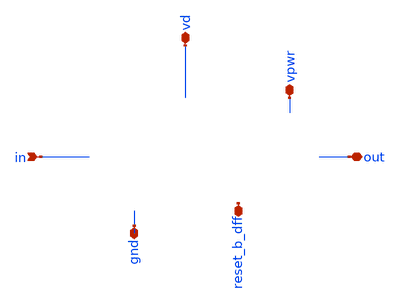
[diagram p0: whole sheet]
** sch_path: sigma-delta_modulator/xschem/sigma-delta-pex.sch
* Copyright 2020 Stefan Frederik Schippers
* Licensed under the Apache License, Version 2.0 (the "License");
* you may not use this file except in compliance with the License.
* You may obtain a copy of the License at
* https://www.apache.org/licenses/LICENSE-2.0
* Unless required by applicable law or agreed to in writing, software
* distributed under the License is distributed on an "AS IS" BASIS,
* WITHOUT WARRANTIES OR CONDITIONS OF ANY KIND, either express or implied.
* See the License for the specific language governing permissions and
* limitations under the License.
**.subckt sigma-delta-pex in gnd out reset_b_dff vpwr vd
*.ipin in
*.iopin gnd
*.iopin out
*.iopin reset_b_dff
*.iopin vpwr
*.iopin vd
**** begin user architecture code



* NGSPICE file created from sigma-delta.ext - technology: sky130A

*.subckt sigma-delta reset_b_dff gnd vd in clk vpwr out
X0 a_n1599_309# a_n1774_335# a_n1420_335# gnd.t15 sky130_fd_pr__nfet_01v8 ad=0.109 pd=1.36 as=0.064
+ ps=0.725 w=0.42 l=0.15
X1 a_n2266_4800# a_n2100_3468# gnd.t37 sky130_fd_pr__res_xhigh_po_0p35 l=4.5
X2 a_n1124_4800# a_n958_3468# gnd.t34 sky130_fd_pr__res_xhigh_po_0p35 l=4.5
X3 x1.Q a_n1599_309# vpwr.t19 vpwr.t18 sky130_fd_pr__pfet_01v8_hvt ad=0.28 pd=2.56 as=0.213 ps=1.67
+ w=1 l=0.15
X4 a_n2339_335# a_n2689_335# a_n2434_335# vpwr.t11 sky130_fd_pr__pfet_01v8_hvt ad=0.0724 pd=0.765
+ as=0.0651 ps=0.73 w=0.42 l=0.15
X5 a_n2121_577# a_n2339_335# vpwr.t13 vpwr.t12 sky130_fd_pr__pfet_01v8_hvt ad=0.129 pd=1.18 as=0.218
+ ps=2.2 w=0.84 l=0.15
X6 a_n1420_335# reset_b_dff.t0 gnd.t7 gnd.t6 sky130_fd_pr__nfet_01v8 ad=0.064 pd=0.725 as=0.125
+ ps=1.01 w=0.42 l=0.15
X7 a_n792_4800# a_n626_3468# gnd.t11 sky130_fd_pr__res_xhigh_po_0p35 l=4.5
X8 in_int gnd.t20 sky130_fd_pr__cap_mim_m3_2 l=27.2 w=27.2
X9 a_n2714_2632# a_n2880_1800# gnd.t19 sky130_fd_pr__res_xhigh_po_0p35 l=2
X10 out.t0 a_n1035_335# gnd.t33 gnd.t32 sky130_fd_pr__nfet_01v8 ad=0.169 pd=1.82 as=0.1 ps=0.985
+ w=0.65 l=0.15
X11 a_n1934_4800# a_n2100_3468# gnd.t35 sky130_fd_pr__res_xhigh_po_0p35 l=4.5
X12 in_comp a_n1884_1800# gnd.t45 sky130_fd_pr__res_xhigh_po_0p35 l=2
X13 a_n1612_701# a_n2689_335# a_n1774_335# vpwr.t10 sky130_fd_pr__pfet_01v8_hvt ad=0.0567 pd=0.69
+ as=0.0588 ps=0.7 w=0.42 l=0.15
X14 a_n2077_335# a_n2121_577# a_n2243_335# gnd.t18 sky130_fd_pr__nfet_01v8 ad=0.0441 pd=0.63 as=0.14
+ ps=1.1 w=0.42 l=0.15
X15 a_n2434_335# x1.D gnd.t17 gnd.t16 sky130_fd_pr__nfet_01v8 ad=0.066 pd=0.745 as=0.221 ps=1.89
+ w=0.42 l=0.15
X16 a_n1599_309# reset_b_dff.t1 vpwr.t1 vpwr.t0 sky130_fd_pr__pfet_01v8_hvt ad=0.0567 pd=0.69
+ as=0.0819 ps=0.81 w=0.42 l=0.15
X17 a_n2598_4800# a_n2764_3468# gnd.t36 sky130_fd_pr__res_xhigh_po_0p35 l=4.5
X18 a_n1665_335# a_n2855_335# a_n1774_335# gnd.t49 sky130_fd_pr__nfet_01v8 ad=0.0669 pd=0.75
+ as=0.0711 ps=0.755 w=0.36 l=0.15
X19 a_n1456_4800# in_int gnd.t14 sky130_fd_pr__res_xhigh_po_0p35 l=4.5
X20 gnd.t31 a_n1599_309# a_n1665_335# gnd.t30 sky130_fd_pr__nfet_01v8 ad=0.125 pd=1.01 as=0.0669
+ ps=0.75 w=0.42 l=0.15
X21 a_n2434_335# x1.D vpwr.t7 vpwr.t6 sky130_fd_pr__pfet_01v8_hvt ad=0.0651 pd=0.73 as=0.109 ps=1.36
+ w=0.42 l=0.15
X22 vpwr.t17 a_n1599_309# a_n1612_701# vpwr.t16 sky130_fd_pr__pfet_01v8_hvt ad=0.0819 pd=0.81
+ as=0.0567 ps=0.69 w=0.42 l=0.15
X23 vpwr.t5 a_n1774_335# a_n1599_309# vpwr.t4 sky130_fd_pr__pfet_01v8_hvt ad=0.213 pd=1.67 as=0.0567
+ ps=0.69 w=0.42 l=0.15
X24 a_n2121_577# a_n2339_335# gnd.t25 gnd.t24 sky130_fd_pr__nfet_01v8 ad=0.0999 pd=0.985 as=0.135
+ ps=1.15 w=0.64 l=0.15
X25 vpwr.t3 clk.t0 a_n2855_335# vpwr.t2 sky130_fd_pr__pfet_01v8_hvt ad=0.0864 pd=0.91 as=0.166
+ ps=1.8 w=0.64 l=0.15
X26 gnd.t53 reset_b_dff.t2 a_n2077_335# gnd.t52 sky130_fd_pr__nfet_01v8 ad=0.135 pd=1.15 as=0.0441
+ ps=0.63 w=0.42 l=0.15
X27 vpwr.t15 a_n1599_309# a_n1035_335# vpwr.t14 sky130_fd_pr__pfet_01v8_hvt ad=0.154 pd=1.34
+ as=0.166 ps=1.8 w=0.64 l=0.15
X28 gnd.t29 a_n1599_309# a_n1035_335# gnd.t28 sky130_fd_pr__nfet_01v8 ad=0.1 pd=0.985 as=0.109
+ ps=1.36 w=0.42 l=0.15
X29 a_n2266_4800# a_n2432_3468# gnd.t2 sky130_fd_pr__res_xhigh_po_0p35 l=4.5
X30 a_n2050_2632# a_n2216_1800# gnd.t1 sky130_fd_pr__res_xhigh_po_0p35 l=2
X31 gnd.t43 clk.t1 a_n2855_335# gnd.t42 sky130_fd_pr__nfet_01v8 ad=0.0567 pd=0.69 as=0.109 ps=1.36
+ w=0.42 l=0.15
X32 a_n2243_335# a_n2689_335# a_n2339_335# gnd.t23 sky130_fd_pr__nfet_01v8 ad=0.14 pd=1.1 as=0.0594
+ ps=0.69 w=0.36 l=0.15
X33 vd.t1 in_comp x1.D vd.t0 sky130_fd_pr__pfet_01v8 ad=0.87 pd=6.58 as=0.87 ps=6.58 w=3 l=0.15
X34 a_n1124_4800# a_n1290_3468# gnd.t44 sky130_fd_pr__res_xhigh_po_0p35 l=4.5
X35 a_n2339_335# a_n2855_335# a_n2434_335# gnd.t48 sky130_fd_pr__nfet_01v8 ad=0.0594 pd=0.69
+ as=0.066 ps=0.745 w=0.36 l=0.15
X36 a_n460_4800# x1.Q gnd.t0 sky130_fd_pr__res_xhigh_po_0p35 l=4.5
X37 a_n2689_335# a_n2855_335# vpwr.t27 vpwr.t26 sky130_fd_pr__pfet_01v8_hvt ad=0.166 pd=1.8
+ as=0.0864 ps=0.91 w=0.64 l=0.15
X38 a_n2231_701# a_n2855_335# a_n2339_335# vpwr.t25 sky130_fd_pr__pfet_01v8_hvt ad=0.116 pd=0.97
+ as=0.0724 ps=0.765 w=0.42 l=0.15
X39 a_n2689_335# a_n2855_335# gnd.t47 gnd.t46 sky130_fd_pr__nfet_01v8 ad=0.109 pd=1.36 as=0.0567
+ ps=0.69 w=0.42 l=0.15
X40 a_n1774_335# a_n2855_335# a_n2121_577# vpwr.t24 sky130_fd_pr__pfet_01v8_hvt ad=0.0588 pd=0.7
+ as=0.129 ps=1.18 w=0.42 l=0.15
X41 a_n2382_2632# a_n2548_1800# gnd.t41 sky130_fd_pr__res_xhigh_po_0p35 l=2
X42 in_int a_n2880_1800# gnd.t13 sky130_fd_pr__res_xhigh_po_0p35 l=2
X43 x1.Q a_n1599_309# gnd.t27 gnd.t26 sky130_fd_pr__nfet_01v8 ad=0.169 pd=1.82 as=0.169 ps=1.82
+ w=0.65 l=0.15
X44 a_n460_4800# a_n626_3468# gnd.t10 sky130_fd_pr__res_xhigh_po_0p35 l=4.5
X45 a_n2231_701# reset_b_dff.t3 vpwr.t23 vpwr.t22 sky130_fd_pr__pfet_01v8_hvt ad=0.109 pd=1.36
+ as=0.0703 ps=0.755 w=0.42 l=0.15
X46 a_n2930_4800# a_n2764_3468# gnd.t5 sky130_fd_pr__res_xhigh_po_0p35 l=4.5
X47 a_n2714_2632# a_n2548_1800# gnd.t9 sky130_fd_pr__res_xhigh_po_0p35 l=2
X48 gnd.t40 in_comp x1.D gnd.t39 sky130_fd_pr__nfet_01v8 ad=0.29 pd=2.58 as=0.29 ps=2.58 w=1 l=0.15
X49 a_n1934_4800# in_int gnd.t21 sky130_fd_pr__res_xhigh_po_0p35 l=4.5
X50 a_n792_4800# a_n958_3468# gnd.t8 sky130_fd_pr__res_xhigh_po_0p35 l=4.5
X51 vpwr.t9 a_n2121_577# a_n2231_701# vpwr.t8 sky130_fd_pr__pfet_01v8_hvt ad=0.0703 pd=0.755
+ as=0.116 ps=0.97 w=0.42 l=0.15
X52 a_n1774_335# a_n2689_335# a_n2121_577# gnd.t22 sky130_fd_pr__nfet_01v8 ad=0.0711 pd=0.755
+ as=0.0999 ps=0.985 w=0.36 l=0.15
X53 a_n2598_4800# a_n2432_3468# gnd.t3 sky130_fd_pr__res_xhigh_po_0p35 l=4.5
X54 a_n2382_2632# a_n2216_1800# gnd.t51 sky130_fd_pr__res_xhigh_po_0p35 l=2
X55 in_comp gnd.t38 sky130_fd_pr__cap_mim_m3_2 l=27.2 w=27.2
X56 a_n2930_4800# in.t0 gnd.t4 sky130_fd_pr__res_xhigh_po_0p35 l=4.5
X57 a_n1456_4800# a_n1290_3468# gnd.t50 sky130_fd_pr__res_xhigh_po_0p35 l=4.5
X58 a_n2050_2632# a_n1884_1800# gnd.t12 sky130_fd_pr__res_xhigh_po_0p35 l=2
X59 out.t1 a_n1035_335# vpwr.t21 vpwr.t20 sky130_fd_pr__pfet_01v8_hvt ad=0.26 pd=2.52 as=0.154
+ ps=1.34 w=1 l=0.15
R0 gnd.n76 gnd.n12 1527.78
R1 gnd.n9 gnd.n3 1273.6
R2 gnd.n10 gnd.n9 1263.33
R3 gnd.t32 gnd.n84 1127.78
R4 gnd.t46 gnd.t16 1049.58
R5 gnd.n84 gnd.n83 788.875
R6 gnd.t26 gnd.t28 773.808
R7 gnd.t15 gnd.t26 773.808
R8 gnd.t23 gnd.t18 683.255
R9 gnd.t30 gnd.t6 613.284
R10 gnd.t52 gnd.t24 543.312
R11 gnd.t22 gnd.t49 448.644
R12 gnd.t24 gnd.t22 407.485
R13 gnd.t28 gnd.t32 399.252
R14 gnd.t49 gnd.t30 395.137
R15 gnd.t48 gnd.t23 395.137
R16 gnd.t16 gnd.t48 391.021
R17 gnd.t6 gnd.t15 374.557
R18 gnd.t42 gnd.t46 345.745
R19 gnd.t18 gnd.t52 296.353
R20 gnd gnd.t42 267.541
R21 gnd.n12 gnd.t0 243.835
R22 gnd.n23 gnd.t17 215.036
R23 gnd.t0 gnd.t10 172.754
R24 gnd.t10 gnd.t11 172.754
R25 gnd.t11 gnd.t8 172.754
R26 gnd.t8 gnd.t34 172.754
R27 gnd.t34 gnd.t44 172.754
R28 gnd.t44 gnd.t50 172.754
R29 gnd.n7 gnd.t45 165.469
R30 gnd.n32 gnd.t27 154.317
R31 gnd.n81 gnd.n1 149.835
R32 gnd.n81 gnd.n80 149.835
R33 gnd.n34 gnd.n33 128.757
R34 gnd.t35 gnd.t1 120.719
R35 gnd.t37 gnd.t51 120.719
R36 gnd.t2 gnd.t41 120.719
R37 gnd.t3 gnd.t9 120.719
R38 gnd.t36 gnd.t19 120.719
R39 gnd.t5 gnd.t13 120.719
R40 gnd.n30 gnd.n29 116.754
R41 gnd.n62 gnd.n21 107.24
R42 gnd.n49 gnd.n48 107.24
R43 gnd.n7 gnd.t14 107.191
R44 gnd.n29 gnd.t7 100.001
R45 gnd.n80 gnd.n78 98.6358
R46 gnd.t21 gnd.n4 93.6618
R47 gnd.n48 gnd.t53 72.8576
R48 gnd.n29 gnd.t31 70.0005
R49 gnd.n48 gnd.t25 60.5809
R50 gnd.n33 gnd.t29 57.1434
R51 gnd.t45 gnd.t21 52.0346
R52 gnd.t12 gnd.t35 52.0346
R53 gnd.t1 gnd.t37 52.0346
R54 gnd.t51 gnd.t2 52.0346
R55 gnd.t41 gnd.t3 52.0346
R56 gnd.t9 gnd.t36 52.0346
R57 gnd.t19 gnd.t5 52.0346
R58 gnd.t13 gnd.t4 52.0346
R59 gnd.n21 gnd.t47 38.5719
R60 gnd.n21 gnd.t43 38.5719
R61 gnd.n37 gnd.n36 34.6358
R62 gnd.n38 gnd.n37 34.6358
R63 gnd.n42 gnd.n41 34.6358
R64 gnd.n43 gnd.n42 34.6358
R65 gnd.n43 gnd.n27 34.6358
R66 gnd.n47 gnd.n27 34.6358
R67 gnd.n51 gnd.n50 34.6358
R68 gnd.n51 gnd.n25 34.6358
R69 gnd.n55 gnd.n25 34.6358
R70 gnd.n56 gnd.n55 34.6358
R71 gnd.n57 gnd.n56 34.6358
R72 gnd.n61 gnd.n23 29.7417
R73 gnd.n36 gnd.n32 27.8593
R74 gnd.n4 gnd.t12 27.0582
R75 gnd.n33 gnd.t33 25.4291
R76 gnd.n63 gnd.n62 24.4919
R77 gnd.n62 gnd.n61 22.9652
R78 gnd.n38 gnd.n30 17.6946
R79 gnd.n16 gnd.t40 17.405
R80 gnd.n57 gnd.n23 14.6829
R81 gnd.n34 gnd.n32 10.9075
R82 gnd.n16 gnd.n15 9.33321
R83 gnd.n50 gnd.n49 7.90638
R84 gnd.n50 gnd.n26 4.6505
R85 gnd.n59 gnd.n23 4.6505
R86 gnd.n62 gnd.n22 4.6505
R87 gnd.n52 gnd.n51 4.6505
R88 gnd.n53 gnd.n25 4.6505
R89 gnd.n55 gnd.n54 4.6505
R90 gnd.n56 gnd.n24 4.6505
R91 gnd.n58 gnd.n57 4.6505
R92 gnd.n61 gnd.n60 4.6505
R93 gnd.n36 gnd.n35 4.6505
R94 gnd.n37 gnd.n31 4.6505
R95 gnd.n39 gnd.n38 4.6505
R96 gnd.n41 gnd.n40 4.6505
R97 gnd.n42 gnd.n28 4.6505
R98 gnd.n44 gnd.n43 4.6505
R99 gnd.n45 gnd.n27 4.6505
R100 gnd.n47 gnd.n46 4.6505
R101 gnd.n65 gnd.n20 4.5005
R102 gnd.n65 gnd.n64 4.5005
R103 gnd.n41 gnd.n30 2.63579
R104 gnd.n65 gnd.n19 2.25328
R105 gnd.n68 gnd.n67 1.93469
R106 gnd.n49 gnd.n47 1.88285
R107 gnd gnd.n66 1.72422
R108 gnd.n68 gnd 1.25931
R109 gnd.n69 gnd.n68 0.575502
R110 gnd.n78 gnd.n77 0.541165
R111 gnd.n77 gnd.n76 0.541165
R112 gnd.n75 gnd.n74 0.347269
R113 gnd.n76 gnd.n75 0.347269
R114 gnd.n67 gnd.t38 0.266467
R115 gnd.n35 gnd.n34 0.144332
R116 gnd.n35 gnd.n31 0.120292
R117 gnd.n39 gnd.n31 0.120292
R118 gnd.n40 gnd.n39 0.120292
R119 gnd.n40 gnd.n28 0.120292
R120 gnd.n44 gnd.n28 0.120292
R121 gnd.n45 gnd.n44 0.120292
R122 gnd.n46 gnd.n45 0.120292
R123 gnd.n46 gnd.n26 0.120292
R124 gnd.n52 gnd.n26 0.120292
R125 gnd.n53 gnd.n52 0.120292
R126 gnd.n54 gnd.n53 0.120292
R127 gnd.n54 gnd.n24 0.120292
R128 gnd.n58 gnd.n24 0.120292
R129 gnd.n59 gnd.n58 0.120292
R130 gnd.n60 gnd.n59 0.120292
R131 gnd.n60 gnd.n22 0.120292
R132 gnd.n1 gnd.n0 0.10956
R133 gnd.n0 gnd.t39 0.10956
R134 gnd.n80 gnd.n79 0.10956
R135 gnd.n73 gnd.n14 0.084913
R136 gnd.n14 gnd.n13 0.0845034
R137 gnd.n22 gnd.n20 0.0734167
R138 gnd.n82 gnd.n81 0.0425017
R139 gnd.n83 gnd.n82 0.0425017
R140 gnd.n64 gnd 0.0330521
R141 gnd.n20 gnd.n18 0.0265417
R142 gnd gnd.n63 0.0226354
R143 gnd.n19 gnd.n18 0.0114272
R144 gnd.n63 gnd.n19 0.0113582
R145 gnd.n66 gnd.n65 0.0110001
R146 gnd.n70 gnd.n16 0.00867757
R147 gnd.n70 gnd.n69 0.00634112
R148 gnd.n64 gnd 0.00570833
R149 gnd.n9 gnd.n8 0.00517349
R150 gnd.n8 gnd.n7 0.00517349
R151 gnd.n6 gnd.n5 0.00517349
R152 gnd.n7 gnd.n6 0.00517349
R153 gnd.n73 gnd.n72 0.00440917
R154 gnd.n3 gnd.n2 0.0043402
R155 gnd.n11 gnd.n10 0.0043402
R156 gnd.n12 gnd.n11 0.0043402
R157 gnd.n72 gnd.n71 0.00391284
R158 gnd.n71 gnd.n70 0.00391159
R159 gnd.n67 gnd.t20 0.00288363
R160 gnd.n66 gnd.n18 0.00100955
R161 gnd.n76 gnd.n73 0.00100353
R162 gnd.n69 gnd.n17 0.00051897
R163 vpwr.t26 vpwr.t6 790.188
R164 vpwr.t18 vpwr.t14 648.131
R165 vpwr.t22 vpwr.t12 583.023
R166 vpwr.n45 vpwr 548.548
R167 vpwr.n26 vpwr.t13 514.011
R168 vpwr.t4 vpwr.t18 485.358
R169 vpwr.t25 vpwr.t8 414.33
R170 vpwr.n2 vpwr.t7 375.277
R171 vpwr.t16 vpwr.t0 319.627
R172 vpwr.n20 vpwr.n9 311.957
R173 vpwr.n42 vpwr.n1 311.894
R174 vpwr.n29 vpwr.n28 309.18
R175 vpwr.t12 vpwr.t24 292.991
R176 vpwr.t11 vpwr.t25 292.991
R177 vpwr.n13 vpwr.n10 292.5
R178 vpwr.n15 vpwr.n14 292.5
R179 vpwr.t14 vpwr.t20 287.072
R180 vpwr.t8 vpwr.t22 287.072
R181 vpwr.t6 vpwr.t11 272.274
R182 vpwr.t24 vpwr.t10 254.518
R183 vpwr.t0 vpwr.t4 248.599
R184 vpwr.t10 vpwr.t16 248.599
R185 vpwr.t2 vpwr.t26 244.306
R186 vpwr vpwr.t2 186.556
R187 vpwr.n14 vpwr.n13 182.929
R188 vpwr.n12 vpwr.n11 148.689
R189 vpwr.n9 vpwr.t17 119.608
R190 vpwr.n28 vpwr.t9 93.81
R191 vpwr.n13 vpwr.t5 68.0124
R192 vpwr.n28 vpwr.t23 63.3219
R193 vpwr.n9 vpwr.t1 63.3219
R194 vpwr.n11 vpwr.t15 61.9158
R195 vpwr.n1 vpwr.t27 41.5552
R196 vpwr.n1 vpwr.t3 41.5552
R197 vpwr.n41 vpwr.n40 34.6358
R198 vpwr.n34 vpwr.n4 34.6358
R199 vpwr.n35 vpwr.n34 34.6358
R200 vpwr.n36 vpwr.n35 34.6358
R201 vpwr.n30 vpwr.n27 34.6358
R202 vpwr.n21 vpwr.n7 34.6358
R203 vpwr.n25 vpwr.n7 34.6358
R204 vpwr.n36 vpwr.n2 32.377
R205 vpwr.n26 vpwr.n25 32.0005
R206 vpwr.n11 vpwr.t21 30.239
R207 vpwr.n20 vpwr.n19 30.1181
R208 vpwr.n14 vpwr.t19 29.316
R209 vpwr.n42 vpwr.n41 22.9652
R210 vpwr.n21 vpwr.n20 20.3299
R211 vpwr.n40 vpwr.n2 18.0711
R212 vpwr.n15 vpwr.n12 13.9946
R213 vpwr.n19 vpwr.n10 12.8758
R214 vpwr.n27 vpwr.n26 9.41227
R215 vpwr.n29 vpwr.n4 6.02403
R216 vpwr.n16 vpwr.n15 5.00414
R217 vpwr.n20 vpwr.n8 4.6505
R218 vpwr.n26 vpwr.n6 4.6505
R219 vpwr.n38 vpwr.n2 4.6505
R220 vpwr.n17 vpwr.n16 4.6505
R221 vpwr.n19 vpwr.n18 4.6505
R222 vpwr.n22 vpwr.n21 4.6505
R223 vpwr.n23 vpwr.n7 4.6505
R224 vpwr.n25 vpwr.n24 4.6505
R225 vpwr.n27 vpwr.n5 4.6505
R226 vpwr.n31 vpwr.n30 4.6505
R227 vpwr.n32 vpwr.n4 4.6505
R228 vpwr.n34 vpwr.n33 4.6505
R229 vpwr.n35 vpwr.n3 4.6505
R230 vpwr.n37 vpwr.n36 4.6505
R231 vpwr.n40 vpwr.n39 4.6505
R232 vpwr.n41 vpwr.n0 4.6505
R233 vpwr.n16 vpwr.n10 4.07323
R234 vpwr.n43 vpwr.n42 3.93272
R235 vpwr.n30 vpwr.n29 3.76521
R236 vpwr vpwr.n51 0.223
R237 vpwr.n17 vpwr.n12 0.144332
R238 vpwr.n43 vpwr.n0 0.138831
R239 vpwr.n18 vpwr.n17 0.120292
R240 vpwr.n18 vpwr.n8 0.120292
R241 vpwr.n22 vpwr.n8 0.120292
R242 vpwr.n23 vpwr.n22 0.120292
R243 vpwr.n24 vpwr.n23 0.120292
R244 vpwr.n24 vpwr.n6 0.120292
R245 vpwr.n6 vpwr.n5 0.120292
R246 vpwr.n31 vpwr.n5 0.120292
R247 vpwr.n32 vpwr.n31 0.120292
R248 vpwr.n33 vpwr.n32 0.120292
R249 vpwr.n33 vpwr.n3 0.120292
R250 vpwr.n37 vpwr.n3 0.120292
R251 vpwr.n38 vpwr.n37 0.120292
R252 vpwr.n39 vpwr.n38 0.120292
R253 vpwr.n39 vpwr.n0 0.120292
R254 vpwr.n44 vpwr.n43 0.107496
R255 vpwr.n47 vpwr 0.088
R256 vpwr.n51 vpwr.n50 0.0197304
R257 vpwr.n44 vpwr 0.0174271
R258 vpwr vpwr.n44 0.01675
R259 vpwr.n48 vpwr.n47 0.013
R260 vpwr.n50 vpwr.n49 0.00412567
R261 vpwr.n49 vpwr.n48 0.003625
R262 vpwr.n50 vpwr.n45 0.0015496
R263 vpwr.n49 vpwr.n46 0.000543305
R264 reset_b_dff.n14 reset_b_dff.t3 413.313
R265 reset_b_dff.n7 reset_b_dff.t1 344.005
R266 reset_b_dff.n6 reset_b_dff.t0 187.321
R267 reset_b_dff.n7 reset_b_dff.n5 152
R268 reset_b_dff.n14 reset_b_dff.t2 126.127
R269 reset_b_dff.n6 reset_b_dff.n1 73.2067
R270 reset_b_dff reset_b_dff.n4 14.0185
R271 reset_b_dff.n11 reset_b_dff.n10 9.3005
R272 reset_b_dff.n8 reset_b_dff.n2 9.3005
R273 reset_b_dff.n8 reset_b_dff.n7 9.3005
R274 reset_b_dff.n7 reset_b_dff.n6 9.15991
R275 reset_b_dff.n15 reset_b_dff.n14 7.02742
R276 reset_b_dff.n4 reset_b_dff 4.7293
R277 reset_b_dff.n9 reset_b_dff.n0 4.6505
R278 reset_b_dff.n18 reset_b_dff.n17 4.6505
R279 reset_b_dff.n4 reset_b_dff 4.53383
R280 reset_b_dff.n5 reset_b_dff 3.11401
R281 reset_b_dff.n17 reset_b_dff.n15 3.0725
R282 reset_b_dff.n24 reset_b_dff 2.98033
R283 reset_b_dff.n12 reset_b_dff 2.36657
R284 reset_b_dff.n5 reset_b_dff.n1 1.55726
R285 reset_b_dff.n10 reset_b_dff.n9 1.55726
R286 reset_b_dff.n8 reset_b_dff.n1 1.38428
R287 reset_b_dff.n9 reset_b_dff.n8 1.38428
R288 reset_b_dff.n10 reset_b_dff 1.38428
R289 reset_b_dff.n17 reset_b_dff.n16 1.2805
R290 reset_b_dff.n12 reset_b_dff 0.580857
R291 reset_b_dff.n3 reset_b_dff 0.196446
R292 reset_b_dff.n20 reset_b_dff 0.171696
R293 reset_b_dff.n20 reset_b_dff.n19 0.0901739
R294 reset_b_dff.n21 reset_b_dff.n20 0.0500874
R295 reset_b_dff.n13 reset_b_dff.n12 0.0466957
R296 reset_b_dff.n26 reset_b_dff.n25 0.0435328
R297 reset_b_dff.n18 reset_b_dff.n13 0.0331087
R298 reset_b_dff.n3 reset_b_dff.n2 0.02675
R299 reset_b_dff reset_b_dff.n11 0.0255
R300 reset_b_dff.n22 reset_b_dff.n21 0.0213989
R301 reset_b_dff.n24 reset_b_dff.n23 0.018111
R302 reset_b_dff.n19 reset_b_dff.n18 0.014087
R303 reset_b_dff.n25 reset_b_dff.n22 0.0127951
R304 reset_b_dff.n11 reset_b_dff.n0 0.01175
R305 reset_b_dff.n2 reset_b_dff.n0 0.0105
R306 reset_b_dff reset_b_dff.n3 0.00725676
R307 reset_b_dff reset_b_dff.n26 0.00459836
R308 reset_b_dff.n25 reset_b_dff.n24 0.0016109
R309 out.n0 out.t1 250.94
R310 out out.t0 144.601
R311 out.n0 out 4.7225
R312 out out.n0 3.35288
R313 clk.n3 clk.t0 294.557
R314 clk.n3 clk.t1 211.01
R315 clk.n4 clk.n3 8.28655
R316 clk.n2 clk 7.73487
R317 clk.n4 clk.n2 1.82961
R318 clk clk.n5 0.981259
R319 clk.n5 clk.n4 0.848973
R320 clk.n0 clk 0.385917
R321 clk.n1 clk.n0 0.03175
R322 clk.n2 clk.n1 0.00111796
R323 vd.n10 vd.n7 135.465
R324 vd.n13 vd.n12 101.647
R325 vd.n26 vd.t1 9.52337
R326 vd vd.n35 4.20467
R327 vd.n14 vd.n13 0.130052
R328 vd.n15 vd.n14 0.130052
R329 vd.n5 vd.n4 0.107375
R330 vd.n15 vd.n5 0.107375
R331 vd.n31 vd.n29 0.0456031
R332 vd.n25 vd.n23 0.0456031
R333 vd.n23 vd.n21 0.0456031
R334 vd.n34 vd.n33 0.0391598
R335 vd.n33 vd.n31 0.0391598
R336 vd.n12 vd.n11 0.0349892
R337 vd.n11 vd.t0 0.0349892
R338 vd.n9 vd.n8 0.0349892
R339 vd.n10 vd.n9 0.0333079
R340 vd.n26 vd.n25 0.0217629
R341 vd.n29 vd.n27 0.0198299
R342 vd.n16 vd.n3 0.0125538
R343 vd.n3 vd.n2 0.0120596
R344 vd.n7 vd.n6 0.00627981
R345 vd.n27 vd.n26 0.00501031
R346 vd.t0 vd.n10 0.00318081
R347 vd.n17 vd.n16 0.0018171
R348 vd.n18 vd.n17 0.00131751
R349 vd.n27 vd.n18 0.00131744
R350 vd.n33 vd.n32 0.00119114
R351 vd.n34 vd.n0 0.00101609
R352 vd.n16 vd.n15 0.00100038
R353 vd.n21 vd.n20 0.00100009
R354 vd.n29 vd.n28 0.000659706
R355 vd.n23 vd.n22 0.000659706
R356 vd.n31 vd.n1 0.000543686
R357 vd.n25 vd.n19 0.000543686
R358 vd.n35 vd.n34 0.000507883
R359 vd.n25 vd.n24 0.000507883
R360 vd.n31 vd.n30 0.000507883
R361 in in.t0 9.56433
C0 a_n1774_335# a_n2121_577# 0.0512f
C1 a_n2548_1800# a_n2714_2632# 0.00938f
C2 a_n1774_335# reset_b_dff 0.239f
C3 a_n1774_335# x1.D 9.45e-19
C4 in a_n2930_4800# 0.0056f
C5 a_n1599_309# reset_b_dff 0.28f
C6 a_n2121_577# vpwr 0.205f
C7 a_n1599_309# x1.D 0.004f
C8 reset_b_dff vpwr 0.205f
C9 a_n2339_335# a_n1774_335# 7.99e-20
C10 x1.D vpwr 0.238f
C11 a_n1124_4800# in_int 0.00765f
C12 a_n2382_2632# in_int 0.0613f
C13 in_comp a_n958_3468# 7.16e-19
C14 a_n1774_335# a_n1612_701# 0.00645f
C15 vd in_comp 0.833f
C16 a_n2339_335# vpwr 0.197f
C17 a_n2548_1800# a_n2880_1800# 0.296f
C18 a_n460_4800# x1.Q 0.00839f
C19 a_n2121_577# a_n1665_335# 4.2e-19
C20 a_n2689_335# a_n1774_335# 0.125f
C21 a_n1612_701# vpwr 7.36e-19
C22 a_n2266_4800# a_n2432_3468# 0.00473f
C23 reset_b_dff a_n1665_335# 7.93e-19
C24 a_n1774_335# out 6.85e-19
C25 x1.D a_n1665_335# 2.42e-20
C26 a_n2598_4800# a_n2432_3468# 0.00482f
C27 a_n1599_309# a_n2689_335# 0.0426f
C28 a_n1599_309# out 0.00735f
C29 a_n2689_335# vpwr 0.57f
C30 x1.Q a_n958_3468# 5e-20
C31 vpwr out 0.584f
C32 x1.Q a_n792_4800# 0.0032f
C33 out a_n2714_2632# 0.00336f
C34 a_n2434_335# clk 3.09e-19
C35 a_n2050_2632# in_comp 0.297f
C36 x1.Q vd 0.186f
C37 reset_b_dff a_n1035_335# 0.00144f
C38 x1.D a_n1035_335# 0.00209f
C39 a_n2855_335# a_n2548_1800# 2.33e-20
C40 x1.Q a_n626_3468# 0.414f
C41 a_n2050_2632# a_n2216_1800# 0.00938f
C42 a_n2548_1800# in_int 0.00497f
C43 a_n1290_3468# a_n958_3468# 0.312f
C44 a_n2100_3468# a_n2432_3468# 0.302f
C45 clk a_n1420_335# 6.32e-21
C46 a_n2855_335# a_n2121_577# 0.0701f
C47 a_n1290_3468# vd 0.00171f
C48 a_n2689_335# a_n1665_335# 2.36e-20
C49 a_n2930_4800# in_int 0.00283f
C50 a_n2855_335# reset_b_dff 0.312f
C51 a_n2434_335# x1.Q 7.58e-20
C52 a_n2855_335# x1.D 0.195f
C53 x1.D in_int 0.0121f
C54 in a_n2432_3468# 4.07e-20
C55 x1.Q a_n2050_2632# 2.81e-19
C56 a_n2880_1800# out 0.0144f
C57 in_comp a_n2216_1800# 4.76e-19
C58 a_n2382_2632# a_n2548_1800# 0.00938f
C59 a_n2689_335# a_n1035_335# 2.01e-19
C60 a_n2339_335# a_n2855_335# 0.115f
C61 a_n1884_1800# a_n2855_335# 1.47e-19
C62 x1.Q a_n1420_335# 6.05e-19
C63 a_n1035_335# out 0.0691f
C64 a_n1884_1800# in_int 0.00497f
C65 x1.Q in_comp 0.425f
C66 clk a_n2077_335# 1.82e-20
C67 a_n2689_335# a_n2855_335# 0.906f
C68 a_n2855_335# out 0.00153f
C69 x1.Q a_n2216_1800# 4.28e-19
C70 a_n2855_335# a_n2243_335# 0.00134f
C71 out in_int 0.0102f
C72 a_n2598_4800# a_n2764_3468# 0.00434f
C73 x1.Q a_n2077_335# 9.75e-20
C74 a_n1774_335# vd 3.52e-19
C75 a_n1599_309# vd 0.00172f
C76 a_n2382_2632# out 0.00336f
C77 vd vpwr 0.00696f
C78 x1.D a_n2548_1800# 3.98e-19
C79 a_n2432_3468# in_int 0.0411f
C80 x1.Q a_n1290_3468# 1.87e-20
C81 a_n2100_3468# a_n2050_2632# 0.00472f
C82 x1.Q a_n2231_701# 3.66e-19
C83 reset_b_dff a_n2121_577# 0.172f
C84 in a_n2764_3468# 0.303f
C85 x1.D a_n2121_577# 6.24e-19
C86 a_n2434_335# vpwr 0.0827f
C87 vd a_n1456_4800# 5.85e-19
C88 a_n2764_3468# a_n2714_2632# 0.00472f
C89 reset_b_dff x1.D 0.223f
C90 vd a_n1934_4800# 6.34e-20
C91 a_n2339_335# a_n2121_577# 0.21f
C92 a_n1599_309# a_n1420_335# 0.0074f
C93 a_n2382_2632# a_n2432_3468# 0.00472f
C94 a_n2339_335# reset_b_dff 0.165f
C95 a_n2689_335# a_n2548_1800# 1.47e-19
C96 a_n2339_335# x1.D 0.00353f
C97 a_n1612_701# a_n2121_577# 2.6e-19
C98 a_n1774_335# in_comp 5.26e-20
C99 a_n460_4800# in_int 0.0109f
C100 a_n2548_1800# out 0.0144f
C101 vd a_n1035_335# 0.00317f
C102 reset_b_dff a_n1612_701# 2.06e-19
C103 a_n1612_701# x1.D 2.11e-20
C104 a_n1774_335# clk 6.46e-20
C105 a_n1599_309# in_comp 0.00158f
C106 a_n2689_335# a_n2121_577# 0.186f
C107 a_n1884_1800# a_n2339_335# 1.87e-19
C108 in_comp vpwr 0.00229f
C109 in_comp a_n2714_2632# 1.21e-19
C110 a_n1599_309# clk 2.68e-20
C111 a_n2121_577# out 3.73e-19
C112 a_n2689_335# reset_b_dff 0.0304f
C113 a_n2689_335# x1.D 0.229f
C114 a_n2243_335# a_n2121_577# 3.16e-19
C115 reset_b_dff out 0.00564f
C116 clk vpwr 0.19f
C117 x1.D out 0.294f
C118 vd a_n2855_335# 1.72e-20
C119 a_n2243_335# reset_b_dff 0.00292f
C120 in_int a_n958_3468# 0.0509f
C121 a_n792_4800# in_int 0.00675f
C122 a_n2243_335# x1.D 8.22e-19
C123 x1.Q a_n2100_3468# 1.43e-21
C124 vd in_int 0.304f
C125 a_n1774_335# x1.Q 0.00593f
C126 a_n2689_335# a_n2339_335# 0.23f
C127 in_int a_n626_3468# 0.0178f
C128 a_n1884_1800# a_n2689_335# 1.07e-19
C129 a_n2339_335# out 7.05e-19
C130 a_n1884_1800# out 0.0144f
C131 a_n1599_309# x1.Q 0.142f
C132 a_n2689_335# a_n1612_701# 1.46e-19
C133 a_n2339_335# a_n2243_335# 0.0138f
C134 a_n2266_4800# a_n2598_4800# 0.303f
C135 x1.Q vpwr 0.175f
C136 a_n2434_335# a_n2855_335# 0.0931f
C137 clk a_n1665_335# 1.1e-20
C138 a_n1124_4800# a_n958_3468# 0.00509f
C139 a_n1124_4800# a_n792_4800# 0.307f
C140 a_n2764_3468# in_int 0.0408f
C141 vd a_n1124_4800# 0.00116f
C142 clk a_n2880_1800# 1.96e-19
C143 a_n2689_335# out 0.0011f
C144 in_comp a_n1035_335# 0.00219f
C145 in a_n1290_3468# 9.87e-22
C146 a_n2050_2632# in_int 0.0597f
C147 a_n2689_335# a_n2243_335# 2.28e-19
C148 vpwr a_n2231_701# 0.143f
C149 x1.Q a_n1665_335# 1.47e-19
C150 a_n2266_4800# a_n2100_3468# 0.00473f
C151 in_comp a_n2855_335# 2.02e-20
C152 in_comp in_int 1.13f
C153 a_n1290_3468# a_n1456_4800# 0.00473f
C154 a_n2382_2632# a_n2050_2632# 0.296f
C155 clk a_n2855_335# 0.273f
C156 x1.Q a_n1035_335# 0.226f
C157 a_n2216_1800# in_int 0.00497f
C158 x1.Q a_n2855_335# 9.54e-19
C159 a_n2382_2632# in_comp 2.91e-19
C160 x1.Q in_int 0.414f
C161 a_n2382_2632# a_n2216_1800# 0.00938f
C162 vd reset_b_dff 2.96e-19
C163 a_n2100_3468# in 1.53e-20
C164 a_n2266_4800# a_n1934_4800# 0.296f
C165 a_n1599_309# a_n1774_335# 0.251f
C166 vd x1.D 0.908f
C167 a_n1774_335# vpwr 0.284f
C168 a_n1290_3468# in_int 0.358f
C169 a_n2855_335# a_n2231_701# 9.73e-19
C170 a_n1599_309# vpwr 0.408f
C171 a_n2930_4800# a_n2764_3468# 0.00458f
C172 a_n1884_1800# vd 1.16e-19
C173 a_n2434_335# reset_b_dff 0.00224f
C174 x1.Q a_n2382_2632# 1.13e-19
C175 a_n2434_335# x1.D 0.164f
C176 a_n1774_335# a_n1665_335# 0.00742f
C177 a_n2100_3468# a_n1934_4800# 0.00434f
C178 a_n2689_335# vd 1.08e-19
C179 a_n2434_335# a_n2339_335# 0.0498f
C180 in_comp a_n2548_1800# 2.76e-19
C181 a_n1290_3468# a_n1124_4800# 0.00536f
C182 a_n2266_4800# in_int 0.00277f
C183 reset_b_dff a_n1420_335# 0.00312f
C184 vd out 0.0503f
C185 a_n1420_335# x1.D 4.54e-20
C186 a_n2598_4800# in_int 0.00321f
C187 a_n2548_1800# a_n2216_1800# 0.296f
C188 a_n1884_1800# a_n2050_2632# 0.00938f
C189 in_comp a_n2121_577# 7.49e-21
C190 a_n1774_335# a_n1035_335# 7.05e-19
C191 in_comp reset_b_dff 4.91e-20
C192 a_n2880_1800# a_n2714_2632# 0.00938f
C193 clk a_n2121_577# 1.78e-19
C194 a_n2434_335# a_n2689_335# 0.0642f
C195 a_n2121_577# a_n2216_1800# 1.53e-19
C196 in_comp x1.D 0.304f
C197 a_n1599_309# a_n1035_335# 0.107f
C198 clk reset_b_dff 0.0302f
C199 reset_b_dff a_n2216_1800# 2.29e-19
C200 vpwr a_n1035_335# 0.198f
C201 clk x1.D 0.0102f
C202 a_n2434_335# a_n2243_335# 4.61e-19
C203 a_n2050_2632# out 0.00336f
C204 a_n2339_335# in_comp 2.02e-20
C205 a_n1884_1800# in_comp 0.0188f
C206 a_n1774_335# a_n2855_335# 0.102f
C207 a_n2100_3468# in_int 0.339f
C208 a_n1934_4800# a_n1456_4800# 0.144f
C209 a_n2077_335# a_n2121_577# 3.69e-19
C210 a_n2339_335# clk 3.26e-19
C211 a_n1884_1800# a_n2216_1800# 0.296f
C212 a_n1599_309# a_n2855_335# 0.0436f
C213 a_n2077_335# reset_b_dff 0.00407f
C214 x1.Q a_n2121_577# 0.00111f
C215 a_n2077_335# x1.D 5.41e-20
C216 a_n1599_309# in_int 0.00137f
C217 x1.Q reset_b_dff 0.0107f
C218 a_n2855_335# vpwr 0.441f
C219 in in_int 0.0139f
C220 x1.Q x1.D 0.0672f
C221 vpwr in_int 0.00515f
C222 in_int a_n2714_2632# 0.399f
C223 a_n2689_335# in_comp 1.41e-20
C224 a_n2339_335# a_n2077_335# 0.00171f
C225 in_comp out 0.0553f
C226 a_n2689_335# clk 0.00241f
C227 a_n2764_3468# a_n2432_3468# 0.296f
C228 a_n2339_335# x1.Q 8.11e-19
C229 clk out 4.76e-19
C230 a_n2216_1800# out 0.0144f
C231 a_n1884_1800# x1.Q 0.00101f
C232 a_n2121_577# a_n2231_701# 0.0977f
C233 clk a_n2243_335# 5.33e-20
C234 reset_b_dff a_n2231_701# 0.013f
C235 a_n460_4800# a_n792_4800# 0.299f
C236 x1.Q a_n1612_701# 4.53e-20
C237 x1.D a_n2231_701# 5.56e-20
C238 a_n460_4800# vd 0.133f
C239 a_n2855_335# a_n1665_335# 2.56e-19
C240 in_int a_n1456_4800# 0.0083f
C241 a_n460_4800# a_n626_3468# 0.00434f
C242 a_n2382_2632# a_n2714_2632# 0.296f
C243 a_n2855_335# a_n2880_1800# 1.68e-19
C244 a_n2689_335# x1.Q 0.00137f
C245 a_n1934_4800# in_int 0.00787f
C246 a_n2339_335# a_n2231_701# 0.0572f
C247 a_n2880_1800# in_int 0.0164f
C248 x1.Q out 0.669f
C249 a_n2598_4800# a_n2930_4800# 0.296f
C250 a_n2855_335# a_n1035_335# 4.71e-20
C251 x1.Q a_n2243_335# 1.45e-19
C252 a_n792_4800# a_n958_3468# 0.00482f
C253 a_n1035_335# in_int 0.00209f
C254 vd a_n958_3468# 0.00352f
C255 vd a_n792_4800# 0.00299f
C256 a_n1124_4800# a_n1456_4800# 0.3f
C257 a_n626_3468# a_n958_3468# 0.303f
C258 a_n792_4800# a_n626_3468# 0.00473f
C259 vd a_n626_3468# 0.0129f
C260 a_n2689_335# a_n2231_701# 0.0346f
C261 out gnd 1.09f
C262 reset_b_dff gnd 1.4f
C263 clk gnd 0.346f
C264 in gnd 0.529f
C265 vd gnd 4.18f
C266 vpwr gnd 2.89f
C267 a_n1420_335# gnd 0.00223f
C268 a_n1665_335# gnd 9.68e-19
C269 a_n2077_335# gnd 0.00579f
C270 a_n2243_335# gnd 0.00863f
C271 a_n2231_701# gnd 0.00469f
C272 a_n2434_335# gnd 0.08f
C273 a_n1035_335# gnd 0.213f
C274 a_n1774_335# gnd 0.275f
C275 a_n1599_309# gnd 0.741f
C276 a_n2339_335# gnd 0.281f
C277 a_n2121_577# gnd 0.194f
C278 a_n2689_335# gnd 0.332f
C279 x1.D gnd 2.59f
C280 a_n2855_335# gnd 0.701f
C281 in_comp gnd 65.9f
C282 a_n1884_1800# gnd 0.549f
C283 a_n2050_2632# gnd 0.331f
C284 a_n2216_1800# gnd 0.349f
C285 a_n2382_2632# gnd 0.331f
C286 a_n2548_1800# gnd 0.349f
C287 a_n2714_2632# gnd 0.331f
C288 a_n2880_1800# gnd 0.53f
C289 x1.Q gnd 1.42f
C290 a_n460_4800# gnd 0.522f
C291 a_n626_3468# gnd 0.354f
C292 a_n792_4800# gnd 0.387f
C293 a_n958_3468# gnd 0.361f
C294 a_n1124_4800# gnd 0.39f
C295 a_n1290_3468# gnd 0.365f
C296 a_n1456_4800# gnd 0.444f
C297 in_int gnd 61.2f
C298 a_n1934_4800# gnd 0.442f
C299 a_n2100_3468# gnd 0.351f
C300 a_n2266_4800# gnd 0.38f
C301 a_n2432_3468# gnd 0.35f
C302 a_n2598_4800# gnd 0.383f
C303 a_n2764_3468# gnd 0.35f
C304 a_n2930_4800# gnd 0.586f
*.ends





.include /foss/pdks/sky130A/libs.ref/sky130_fd_sc_hd/spice/sky130_fd_sc_hd.spice


**** end user architecture code
**.ends
.end
